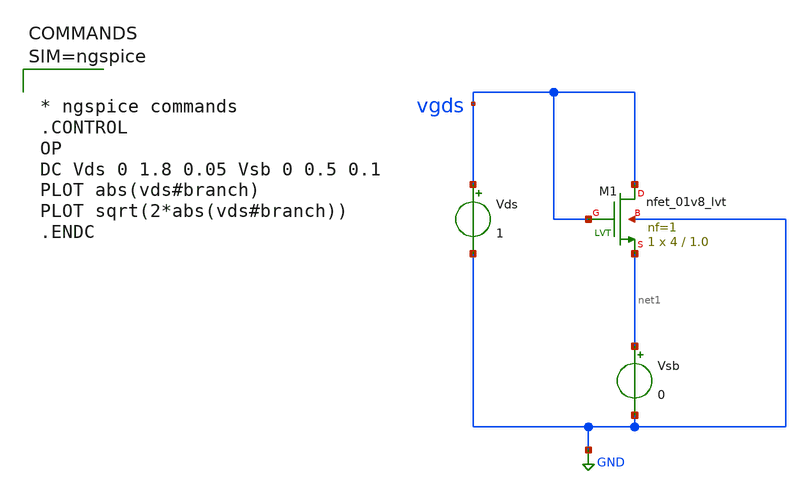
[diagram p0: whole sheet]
** sch_path: work/xschem/untitled-2.sch
**.subckt untitled-2
XM1 vgds vgds net1 GND sky130_fd_pr__nfet_01v8_lvt L=1.0 W=4 nf=1 ad='int((1 + 1)/2) * 4 / 1 * 0.29'
+ as='int((1 + 2)/2) * 4 / 1 * 0.29' pd='2*int((1 + 1)/2) * (4 / 1 + 0.29)' ps='2*int((1 + 2)/2) * (4 / 1 + 0.29)'
+ nrd='0.29 / 4 ' nrs='0.29 / 4 ' sa=0 sb=0 sd=0 mult=1 m=1
Vds vgds GND 1
Vsb net1 GND 0
**** begin user architecture code



* ngspice commands
.CONTROL
OP
DC Vds 0 1.8 0.05 Vsb 0 0.5 0.1
PLOT abs(vds#branch)
PLOT sqrt(2*abs(vds#branch))
.ENDC





** opencircuitdesign pdks install
.lib $::SKYWATER_MODELS/sky130.lib.spice tt

**** end user architecture code
**.ends
.GLOBAL GND
.end
